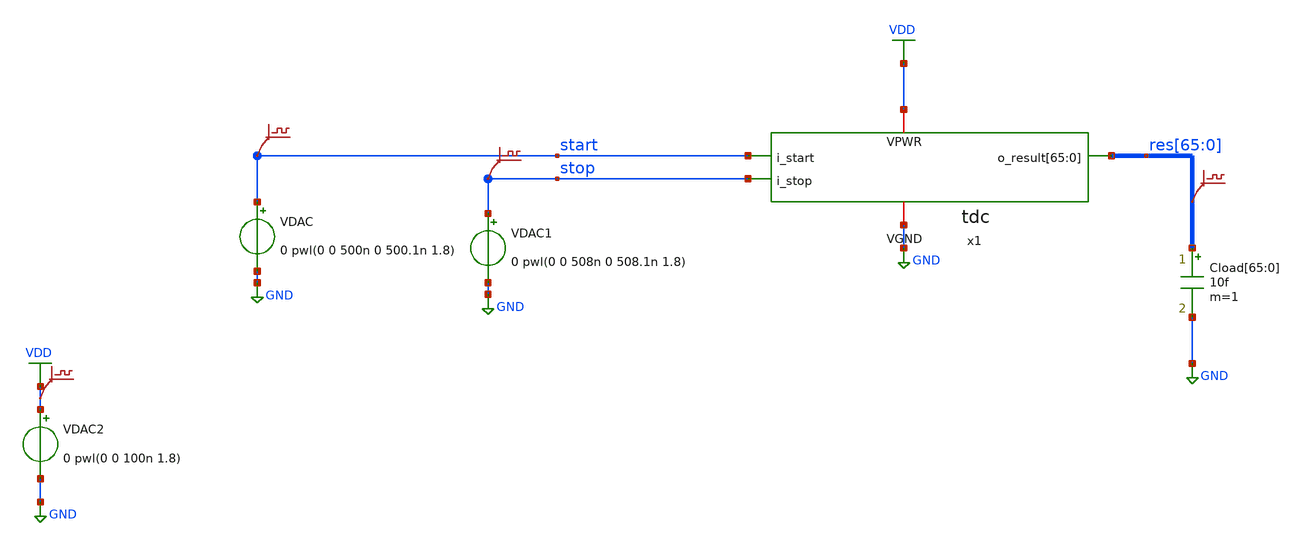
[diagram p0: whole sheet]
** sch_path: sim/tdc_simple/tb_tt06_tdc.sch
**.subckt tb_tt06_tdc
x1 start stop res[65] res[64] res[63] res[62] res[61] res[60] res[59] res[58] res[57] res[56]
+ res[55] res[54] res[53] res[52] res[51] res[50] res[49] res[48] res[47] res[46] res[45] res[44] res[43]
+ res[42] res[41] res[40] res[39] res[38] res[37] res[36] res[35] res[34] res[33] res[32] res[31] res[30]
+ res[29] res[28] res[27] res[26] res[25] res[24] res[23] res[22] res[21] res[20] res[19] res[18] res[17]
+ res[16] res[15] res[14] res[13] res[12] res[11] res[10] res[9] res[8] res[7] res[6] res[5] res[4] res[3]
+ res[2] res[1] res[0] VDD GND tdc
VDAC start GND 0 pwl(0 0 500n 0 500.1n 1.8)
.save v(start)
VDAC1 stop GND 0 pwl(0 0 508n 0 508.1n 1.8)
.save v(stop)
Cload[65] res[65] GND 10f m=1
Cload[64] res[64] GND 10f m=1
Cload[63] res[63] GND 10f m=1
Cload[62] res[62] GND 10f m=1
Cload[61] res[61] GND 10f m=1
Cload[60] res[60] GND 10f m=1
Cload[59] res[59] GND 10f m=1
Cload[58] res[58] GND 10f m=1
Cload[57] res[57] GND 10f m=1
Cload[56] res[56] GND 10f m=1
Cload[55] res[55] GND 10f m=1
Cload[54] res[54] GND 10f m=1
Cload[53] res[53] GND 10f m=1
Cload[52] res[52] GND 10f m=1
Cload[51] res[51] GND 10f m=1
Cload[50] res[50] GND 10f m=1
Cload[49] res[49] GND 10f m=1
Cload[48] res[48] GND 10f m=1
Cload[47] res[47] GND 10f m=1
Cload[46] res[46] GND 10f m=1
Cload[45] res[45] GND 10f m=1
Cload[44] res[44] GND 10f m=1
Cload[43] res[43] GND 10f m=1
Cload[42] res[42] GND 10f m=1
Cload[41] res[41] GND 10f m=1
Cload[40] res[40] GND 10f m=1
Cload[39] res[39] GND 10f m=1
Cload[38] res[38] GND 10f m=1
Cload[37] res[37] GND 10f m=1
Cload[36] res[36] GND 10f m=1
Cload[35] res[35] GND 10f m=1
Cload[34] res[34] GND 10f m=1
Cload[33] res[33] GND 10f m=1
Cload[32] res[32] GND 10f m=1
Cload[31] res[31] GND 10f m=1
Cload[30] res[30] GND 10f m=1
Cload[29] res[29] GND 10f m=1
Cload[28] res[28] GND 10f m=1
Cload[27] res[27] GND 10f m=1
Cload[26] res[26] GND 10f m=1
Cload[25] res[25] GND 10f m=1
Cload[24] res[24] GND 10f m=1
Cload[23] res[23] GND 10f m=1
Cload[22] res[22] GND 10f m=1
Cload[21] res[21] GND 10f m=1
Cload[20] res[20] GND 10f m=1
Cload[19] res[19] GND 10f m=1
Cload[18] res[18] GND 10f m=1
Cload[17] res[17] GND 10f m=1
Cload[16] res[16] GND 10f m=1
Cload[15] res[15] GND 10f m=1
Cload[14] res[14] GND 10f m=1
Cload[13] res[13] GND 10f m=1
Cload[12] res[12] GND 10f m=1
Cload[11] res[11] GND 10f m=1
Cload[10] res[10] GND 10f m=1
Cload[9] res[9] GND 10f m=1
Cload[8] res[8] GND 10f m=1
Cload[7] res[7] GND 10f m=1
Cload[6] res[6] GND 10f m=1
Cload[5] res[5] GND 10f m=1
Cload[4] res[4] GND 10f m=1
Cload[3] res[3] GND 10f m=1
Cload[2] res[2] GND 10f m=1
Cload[1] res[1] GND 10f m=1
Cload[0] res[0] GND 10f m=1
.save v(res[65])
.save v(res[64])
.save v(res[63])
.save v(res[62])
.save v(res[61])
.save v(res[60])
.save v(res[59])
.save v(res[58])
.save v(res[57])
.save v(res[56])
.save v(res[55])
.save v(res[54])
.save v(res[53])
.save v(res[52])
.save v(res[51])
.save v(res[50])
.save v(res[49])
.save v(res[48])
.save v(res[47])
.save v(res[46])
.save v(res[45])
.save v(res[44])
.save v(res[43])
.save v(res[42])
.save v(res[41])
.save v(res[40])
.save v(res[39])
.save v(res[38])
.save v(res[37])
.save v(res[36])
.save v(res[35])
.save v(res[34])
.save v(res[33])
.save v(res[32])
.save v(res[31])
.save v(res[30])
.save v(res[29])
.save v(res[28])
.save v(res[27])
.save v(res[26])
.save v(res[25])
.save v(res[24])
.save v(res[23])
.save v(res[22])
.save v(res[21])
.save v(res[20])
.save v(res[19])
.save v(res[18])
.save v(res[17])
.save v(res[16])
.save v(res[15])
.save v(res[14])
.save v(res[13])
.save v(res[12])
.save v(res[11])
.save v(res[10])
.save v(res[9])
.save v(res[8])
.save v(res[7])
.save v(res[6])
.save v(res[5])
.save v(res[4])
.save v(res[3])
.save v(res[2])
.save v(res[1])
.save v(res[0])
.save v(vdd)
VDAC2 VDD GND 0 pwl(0 0 100n 1.8)
**** begin user architecture code



* ngspice commands
****************

.save v(x1.w_dly_sig[0])
.save v(x1.w_dly_sig[1])
.save v(x1.w_dly_sig[2])
.save v(x1.w_dly_sig[3])
.save v(x1.w_dly_sig[4])
.save v(x1.w_dly_sig[5])
.save v(x1.w_dly_sig[6])
.save v(x1.w_dly_sig[7])
.save v(x1.w_dly_sig[8])
.save v(x1.w_dly_sig[9])
.save v(x1.w_dly_sig[10])
.save v(x1.w_dly_sig[11])
.save v(x1.w_dly_sig[12])
.save v(x1.w_dly_sig[13])
.save v(x1.w_dly_sig[14])
.save v(x1.w_dly_sig[15])
.save v(x1.w_dly_sig[16])
.save v(x1.w_dly_sig[17])
.save v(x1.w_dly_sig[18])
.save v(x1.w_dly_sig[19])
.save v(x1.w_dly_sig[20])
.save v(x1.w_dly_sig[21])

****************
* Misc
****************
.param fclk=10MEG
.options method=gear maxord=2
.temp 30

.control
set num_threads=6
tran 0.01n 600n

write tb_tt06_tdc.raw

*exit
.endc




** opencircuitdesign pdks install
.lib $::SKYWATER_MODELS/sky130.lib.spice tt


**** end user architecture code
**.ends

* expanding   symbol:  tdc.sym # of pins=5
** sym_path: sim/tdc_simple/tdc.sym
.include tdc.pex.spice
.GLOBAL VDD
.GLOBAL GND
.end
